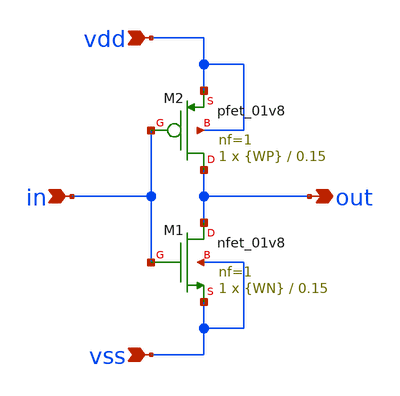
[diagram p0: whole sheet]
** sch_path: eamta2021/sch/inv/inv.sch
**.subckt inv vdd vss in out
*.ipin vdd
*.ipin vss
*.ipin in
*.opin out
XM1 out in vss vss sky130_fd_pr__nfet_01v8 L=0.15 W={WN} nf=1 ad='int((nf+1)/2) * W/nf * 0.29' as='int((nf+2)/2) * W/nf * 0.29'
+ pd='2*int((nf+1)/2) * (W/nf + 0.29)' ps='2*int((nf+2)/2) * (W/nf + 0.29)' nrd='0.29 / W' nrs='0.29 / W'
+ sa=0 sb=0 sd=0 mult=1 m=1
XM2 out in vdd vdd sky130_fd_pr__pfet_01v8 L=0.15 W={WP} nf=1 ad='int((nf+1)/2) * W/nf * 0.29' as='int((nf+2)/2) * W/nf * 0.29'
+ pd='2*int((nf+1)/2) * (W/nf + 0.29)' ps='2*int((nf+2)/2) * (W/nf + 0.29)' nrd='0.29 / W' nrs='0.29 / W'
+ sa=0 sb=0 sd=0 mult=1 m=1
**.ends
.end
